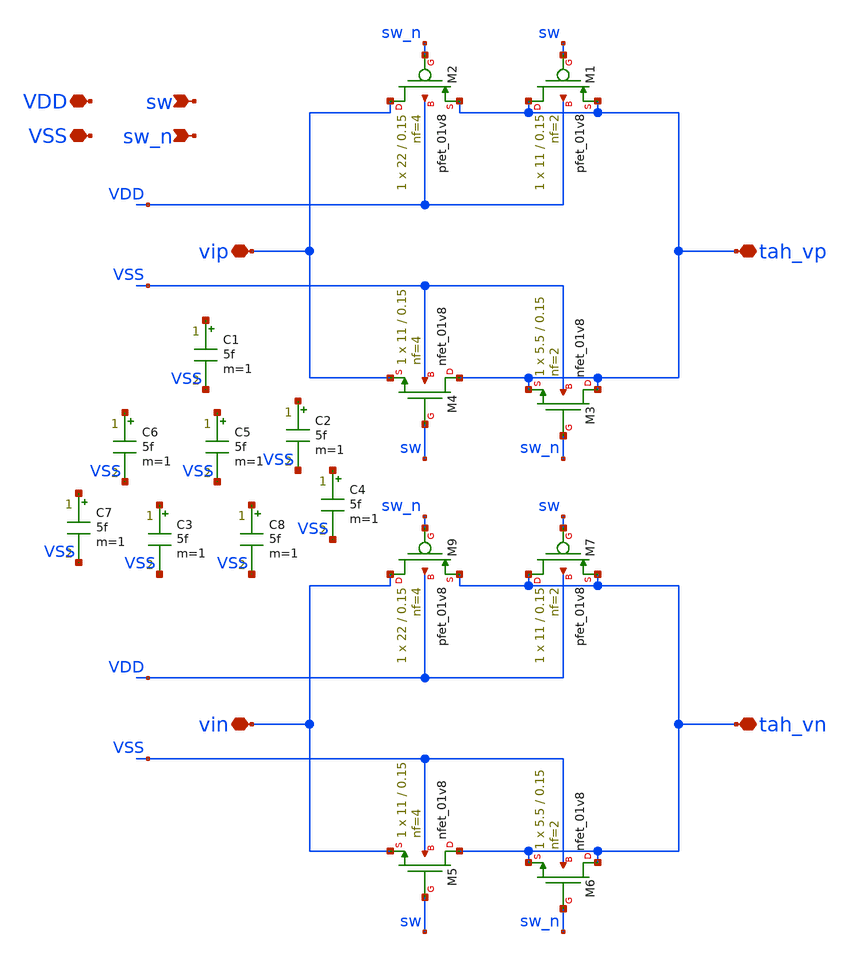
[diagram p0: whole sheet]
** sch_path: hgu/xschem/hgu_tah.sch
**.subckt hgu_tah tah_vp vip VDD VSS sw sw_n tah_vn vin
*.iopin tah_vp
*.iopin vip
*.iopin VDD
*.iopin VSS
*.ipin sw
*.ipin sw_n
*.iopin tah_vn
*.iopin vin
XM1 tah_vp sw tah_vp VDD sky130_fd_pr__pfet_01v8 L=0.15 W=11 nf=2 ad='int((nf+1)/2) * W/nf * 0.29' as='int((nf+2)/2) * W/nf * 0.29'
+ pd='2*int((nf+1)/2) * (W/nf + 0.29)' ps='2*int((nf+2)/2) * (W/nf + 0.29)' nrd='0.29 / W' nrs='0.29 / W'
+ sa=0 sb=0 sd=0 mult=1 m=1
XM4 tah_vp sw vip VSS sky130_fd_pr__nfet_01v8 L=0.15 W=11 nf=4 ad='int((nf+1)/2) * W/nf * 0.29' as='int((nf+2)/2) * W/nf * 0.29'
+ pd='2*int((nf+1)/2) * (W/nf + 0.29)' ps='2*int((nf+2)/2) * (W/nf + 0.29)' nrd='0.29 / W' nrs='0.29 / W'
+ sa=0 sb=0 sd=0 mult=1 m=1
XM2 vip sw_n tah_vp VDD sky130_fd_pr__pfet_01v8 L=0.15 W=22 nf=4 ad='int((nf+1)/2) * W/nf * 0.29' as='int((nf+2)/2) * W/nf * 0.29'
+ pd='2*int((nf+1)/2) * (W/nf + 0.29)' ps='2*int((nf+2)/2) * (W/nf + 0.29)' nrd='0.29 / W' nrs='0.29 / W'
+ sa=0 sb=0 sd=0 mult=1 m=1
XM3 tah_vp sw_n tah_vp VSS sky130_fd_pr__nfet_01v8 L=0.15 W=5.5 nf=2 ad='int((nf+1)/2) * W/nf * 0.29'
+ as='int((nf+2)/2) * W/nf * 0.29' pd='2*int((nf+1)/2) * (W/nf + 0.29)' ps='2*int((nf+2)/2) * (W/nf + 0.29)'
+ nrd='0.29 / W' nrs='0.29 / W' sa=0 sb=0 sd=0 mult=1 m=1
XM9 vin sw_n tah_vn VDD sky130_fd_pr__pfet_01v8 L=0.15 W=22 nf=4 ad='int((nf+1)/2) * W/nf * 0.29' as='int((nf+2)/2) * W/nf * 0.29'
+ pd='2*int((nf+1)/2) * (W/nf + 0.29)' ps='2*int((nf+2)/2) * (W/nf + 0.29)' nrd='0.29 / W' nrs='0.29 / W'
+ sa=0 sb=0 sd=0 mult=1 m=1
XM7 tah_vn sw tah_vn VDD sky130_fd_pr__pfet_01v8 L=0.15 W=11 nf=2 ad='int((nf+1)/2) * W/nf * 0.29' as='int((nf+2)/2) * W/nf * 0.29'
+ pd='2*int((nf+1)/2) * (W/nf + 0.29)' ps='2*int((nf+2)/2) * (W/nf + 0.29)' nrd='0.29 / W' nrs='0.29 / W'
+ sa=0 sb=0 sd=0 mult=1 m=1
XM5 tah_vn sw vin VSS sky130_fd_pr__nfet_01v8 L=0.15 W=11 nf=4 ad='int((nf+1)/2) * W/nf * 0.29' as='int((nf+2)/2) * W/nf * 0.29'
+ pd='2*int((nf+1)/2) * (W/nf + 0.29)' ps='2*int((nf+2)/2) * (W/nf + 0.29)' nrd='0.29 / W' nrs='0.29 / W'
+ sa=0 sb=0 sd=0 mult=1 m=1
XM6 tah_vn sw_n tah_vn VSS sky130_fd_pr__nfet_01v8 L=0.15 W=5.5 nf=2 ad='int((nf+1)/2) * W/nf * 0.29'
+ as='int((nf+2)/2) * W/nf * 0.29' pd='2*int((nf+1)/2) * (W/nf + 0.29)' ps='2*int((nf+2)/2) * (W/nf + 0.29)'
+ nrd='0.29 / W' nrs='0.29 / W' sa=0 sb=0 sd=0 mult=1 m=1
C1 net1 VSS 5f m=1
C2 net2 VSS 5f m=1
C3 net3 VSS 5f m=1
C4 net4 VSS 5f m=1
C5 net5 VSS 5f m=1
C6 net6 VSS 5f m=1
C7 net7 VSS 5f m=1
C8 net8 VSS 5f m=1
**.ends
.end
